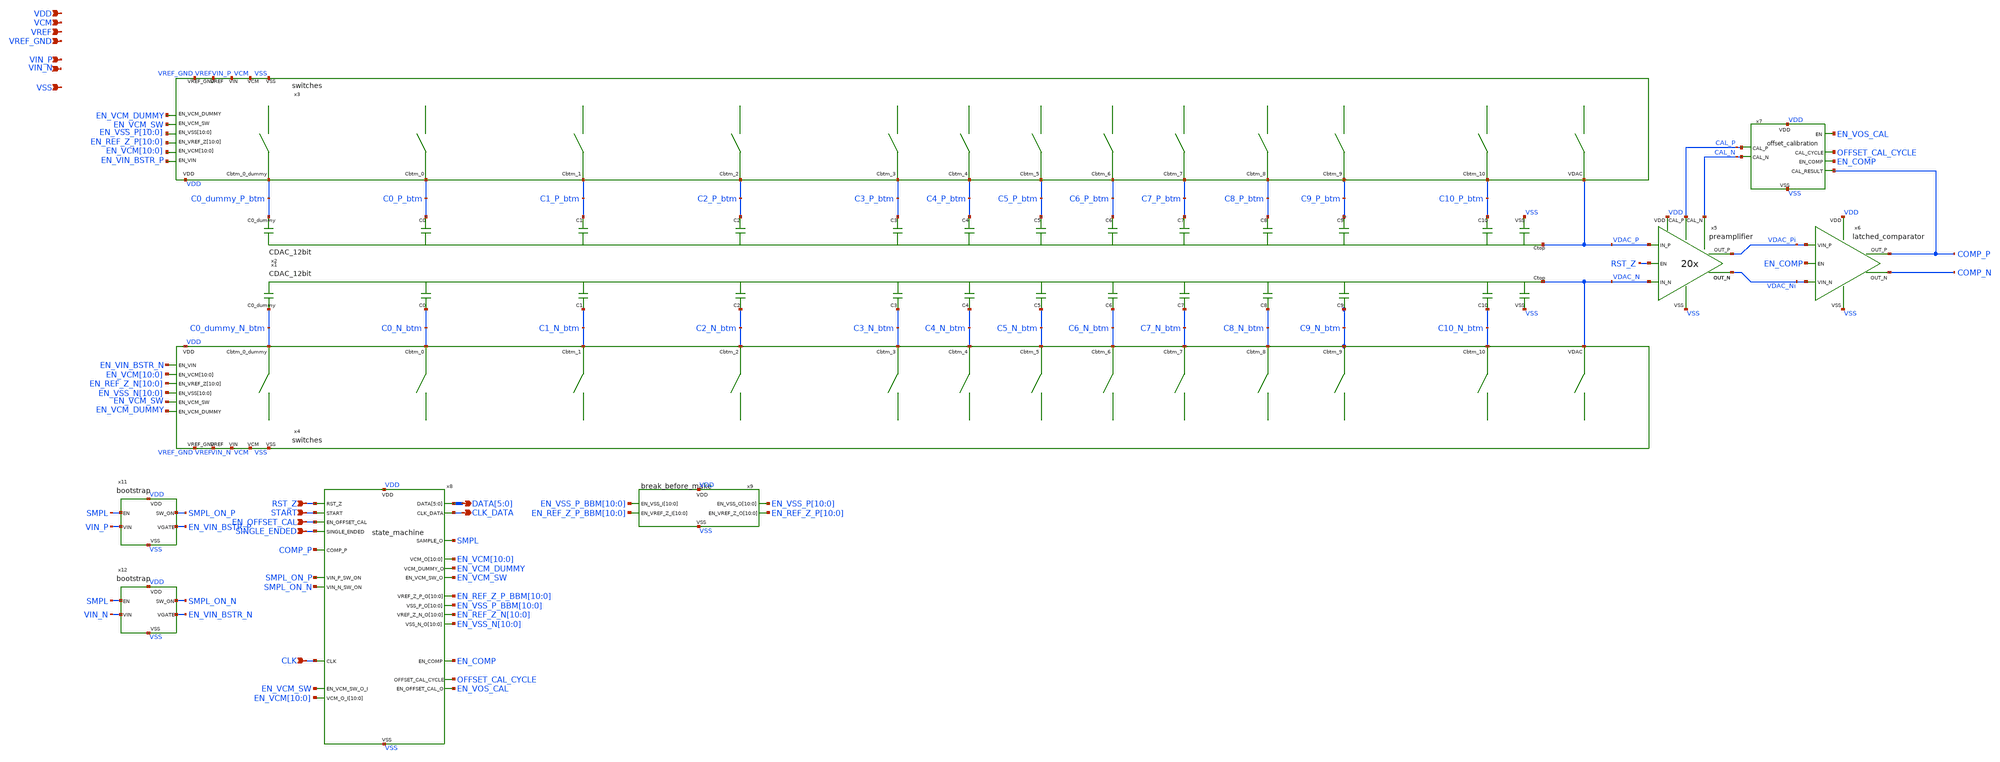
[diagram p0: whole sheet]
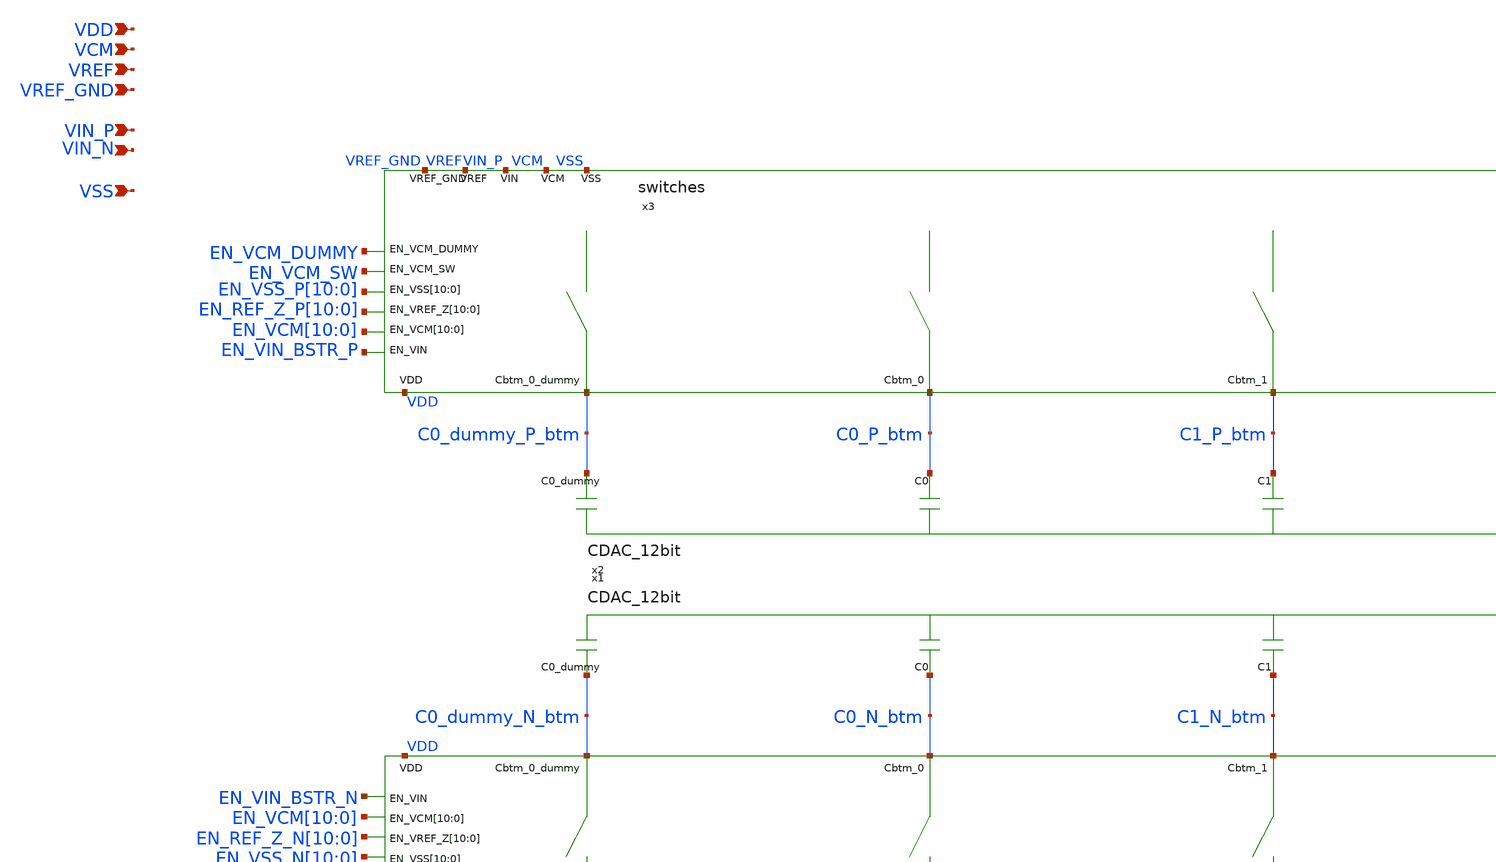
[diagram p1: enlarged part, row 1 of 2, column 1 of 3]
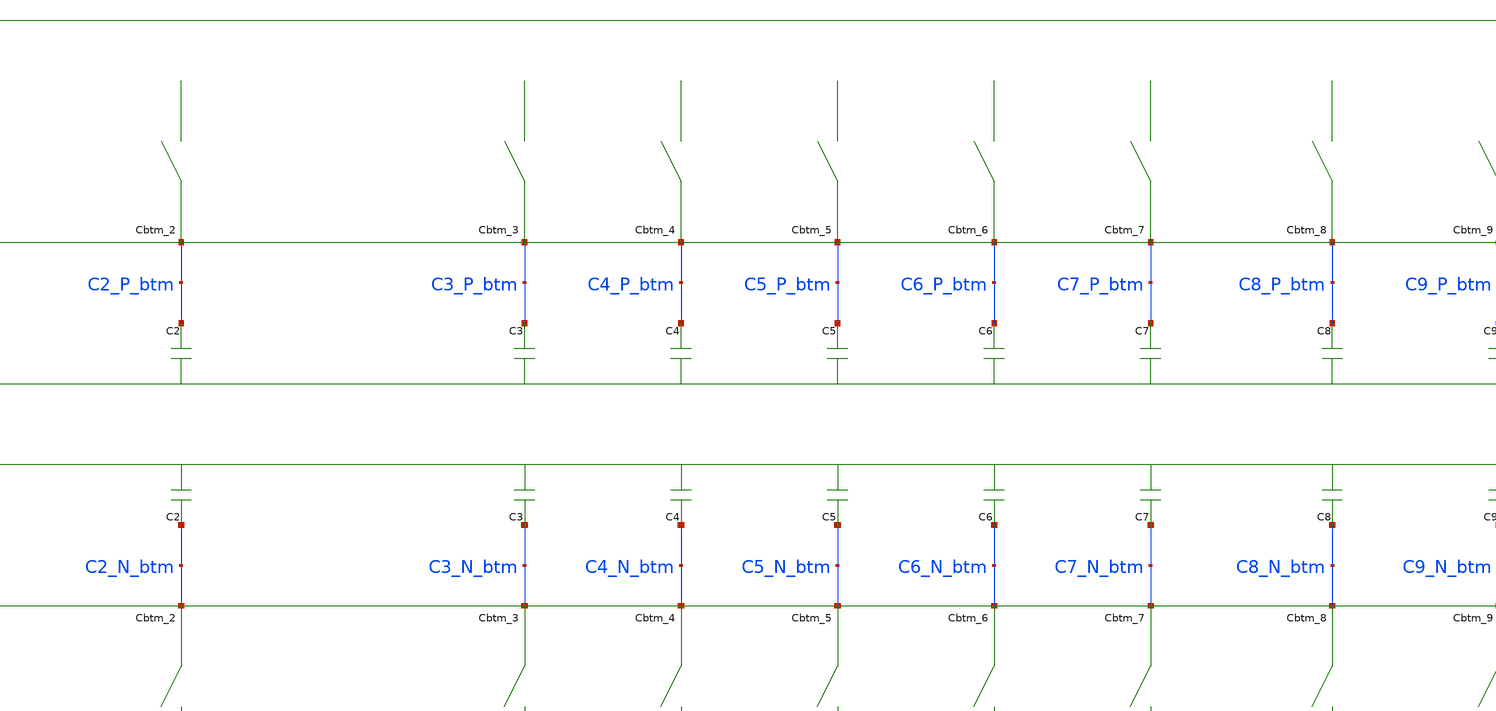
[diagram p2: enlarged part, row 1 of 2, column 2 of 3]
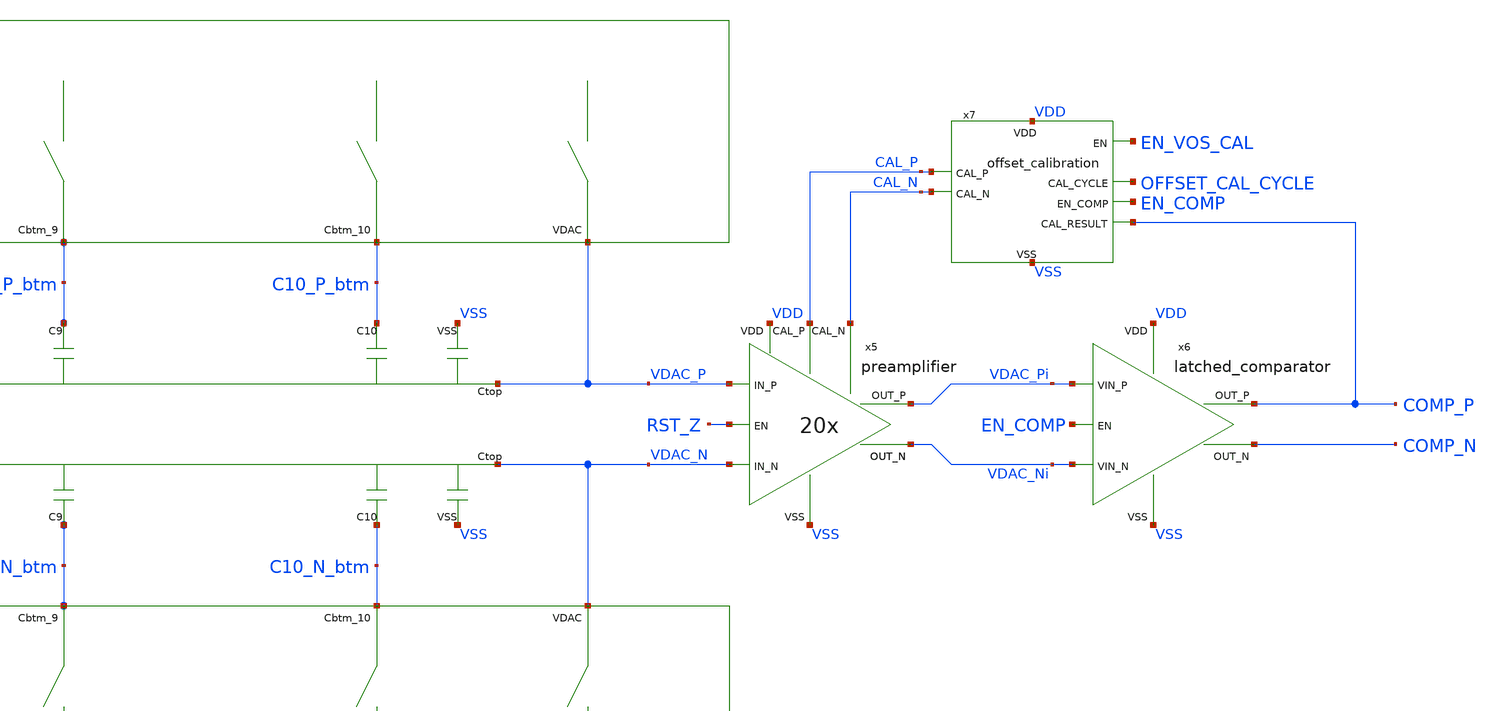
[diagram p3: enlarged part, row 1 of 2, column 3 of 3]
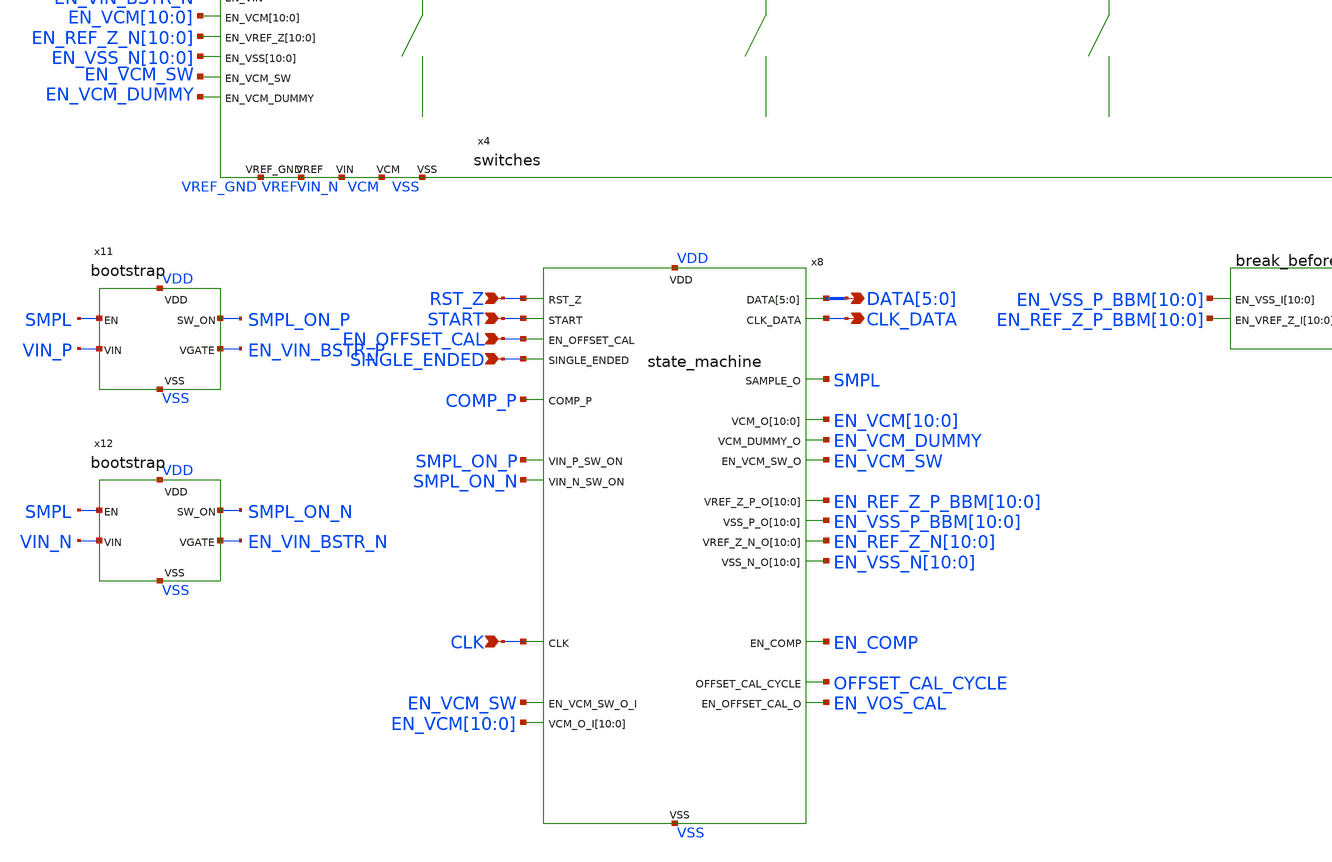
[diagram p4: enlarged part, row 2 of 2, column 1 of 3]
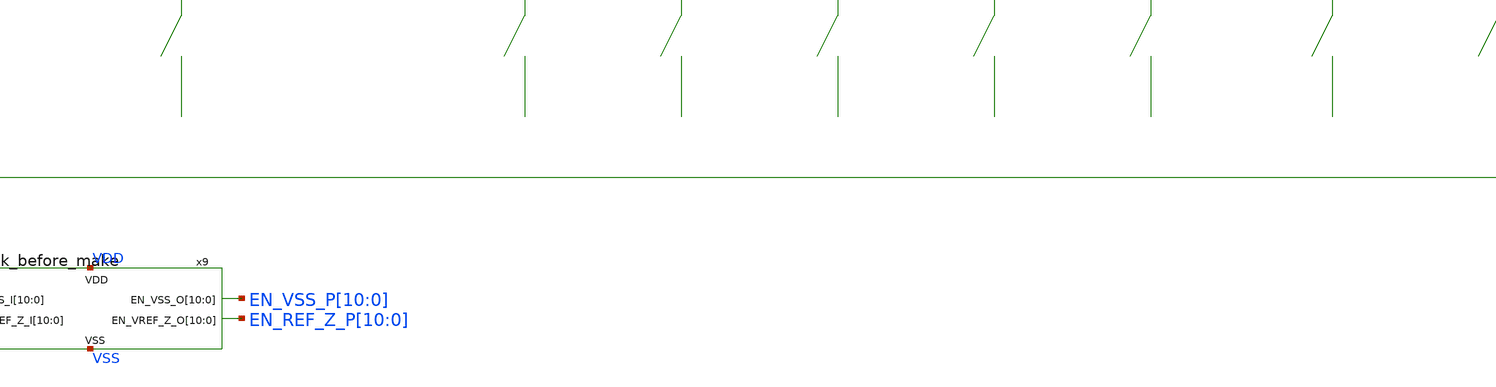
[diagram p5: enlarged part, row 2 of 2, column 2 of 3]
** sch_path: schematic/SAR_ADC_12bit.sch
**.subckt SAR_ADC_12bit VIN_P VDD VREF VCM VSS VIN_N RST_Z START CLK_DATA
*+ DATA[5],DATA[4],DATA[3],DATA[2],DATA[1],DATA[0] EN_OFFSET_CAL CLK VREF_GND SINGLE_ENDED
*.ipin VIN_P
*.ipin VDD
*.ipin VREF
*.ipin VCM
*.ipin VSS
*.ipin VIN_N
*.ipin RST_Z
*.ipin START
*.opin CLK_DATA
*.opin DATA[5],DATA[4],DATA[3],DATA[2],DATA[1],DATA[0]
*.ipin EN_OFFSET_CAL
*.ipin CLK
*.ipin VREF_GND
*.ipin SINGLE_ENDED
x1 C0_dummy_N_btm C0_N_btm C1_N_btm C2_N_btm C3_N_btm C4_N_btm C5_N_btm C6_N_btm C7_N_btm C8_N_btm
+ C9_N_btm C10_N_btm VDAC_N VSS CDAC_12bit
x2 C0_dummy_P_btm C0_P_btm C1_P_btm C2_P_btm C3_P_btm C4_P_btm C5_P_btm C6_P_btm C7_P_btm C8_P_btm
+ C9_P_btm C10_P_btm VDAC_P VSS CDAC_12bit
x3 VCM VREF_GND VREF VIN_P EN_VIN_BSTR_P EN_REF_Z_P[10] EN_REF_Z_P[9] EN_REF_Z_P[8] EN_REF_Z_P[7]
+ EN_REF_Z_P[6] EN_REF_Z_P[5] EN_REF_Z_P[4] EN_REF_Z_P[3] EN_REF_Z_P[2] EN_REF_Z_P[1] EN_REF_Z_P[0] EN_VSS_P[10]
+ EN_VSS_P[9] EN_VSS_P[8] EN_VSS_P[7] EN_VSS_P[6] EN_VSS_P[5] EN_VSS_P[4] EN_VSS_P[3] EN_VSS_P[2] EN_VSS_P[1]
+ EN_VSS_P[0] EN_VCM[10] EN_VCM[9] EN_VCM[8] EN_VCM[7] EN_VCM[6] EN_VCM[5] EN_VCM[4] EN_VCM[3] EN_VCM[2]
+ EN_VCM[1] EN_VCM[0] EN_VCM_SW EN_VCM_DUMMY C8_P_btm C7_P_btm C0_P_btm C6_P_btm C5_P_btm C0_dummy_P_btm
+ C4_P_btm C3_P_btm VDAC_P C10_P_btm C9_P_btm C2_P_btm C1_P_btm VDD VSS switches
x4 VCM VREF_GND VREF VIN_N EN_VIN_BSTR_N EN_REF_Z_N[10] EN_REF_Z_N[9] EN_REF_Z_N[8] EN_REF_Z_N[7]
+ EN_REF_Z_N[6] EN_REF_Z_N[5] EN_REF_Z_N[4] EN_REF_Z_N[3] EN_REF_Z_N[2] EN_REF_Z_N[1] EN_REF_Z_N[0] EN_VSS_N[10]
+ EN_VSS_N[9] EN_VSS_N[8] EN_VSS_N[7] EN_VSS_N[6] EN_VSS_N[5] EN_VSS_N[4] EN_VSS_N[3] EN_VSS_N[2] EN_VSS_N[1]
+ EN_VSS_N[0] EN_VCM[10] EN_VCM[9] EN_VCM[8] EN_VCM[7] EN_VCM[6] EN_VCM[5] EN_VCM[4] EN_VCM[3] EN_VCM[2]
+ EN_VCM[1] EN_VCM[0] EN_VCM_SW EN_VCM_DUMMY C8_N_btm C7_N_btm C0_N_btm C6_N_btm C5_N_btm C0_dummy_N_btm
+ C4_N_btm C3_N_btm VDAC_N C10_N_btm C9_N_btm C2_N_btm C1_N_btm VDD VSS switches
x5 VDAC_N VDAC_P VDD RST_Z VDAC_Pi VDAC_Ni VSS CAL_P CAL_N preamplifier
x6 VDD VDAC_Pi VDAC_Ni EN_COMP COMP_P COMP_N VSS latched_comparator
x7 VDD COMP_P EN_COMP CAL_P CAL_N EN_VOS_CAL VSS OFFSET_CAL_CYCLE offset_calibration
x8 VDD VSS RST_Z START COMP_P SMPL EN_VCM[10] EN_VCM[9] EN_VCM[8] EN_VCM[7] EN_VCM[6] EN_VCM[5]
+ EN_VCM[4] EN_VCM[3] EN_VCM[2] EN_VCM[1] EN_VCM[0] EN_COMP SMPL_ON_P SMPL_ON_N EN_VCM_DUMMY EN_VCM_SW
+ EN_OFFSET_CAL OFFSET_CAL_CYCLE EN_VOS_CAL CLK_DATA DATA[5] DATA[4] DATA[3] DATA[2] DATA[1] DATA[0] EN_VSS_N[10]
+ EN_VSS_N[9] EN_VSS_N[8] EN_VSS_N[7] EN_VSS_N[6] EN_VSS_N[5] EN_VSS_N[4] EN_VSS_N[3] EN_VSS_N[2] EN_VSS_N[1]
+ EN_VSS_N[0] EN_REF_Z_N[10] EN_REF_Z_N[9] EN_REF_Z_N[8] EN_REF_Z_N[7] EN_REF_Z_N[6] EN_REF_Z_N[5] EN_REF_Z_N[4]
+ EN_REF_Z_N[3] EN_REF_Z_N[2] EN_REF_Z_N[1] EN_REF_Z_N[0] EN_VSS_P_BBM[10] EN_VSS_P_BBM[9] EN_VSS_P_BBM[8]
+ EN_VSS_P_BBM[7] EN_VSS_P_BBM[6] EN_VSS_P_BBM[5] EN_VSS_P_BBM[4] EN_VSS_P_BBM[3] EN_VSS_P_BBM[2] EN_VSS_P_BBM[1]
+ EN_VSS_P_BBM[0] EN_REF_Z_P_BBM[10] EN_REF_Z_P_BBM[9] EN_REF_Z_P_BBM[8] EN_REF_Z_P_BBM[7] EN_REF_Z_P_BBM[6]
+ EN_REF_Z_P_BBM[5] EN_REF_Z_P_BBM[4] EN_REF_Z_P_BBM[3] EN_REF_Z_P_BBM[2] EN_REF_Z_P_BBM[1] EN_REF_Z_P_BBM[0] CLK
+ EN_VCM_SW EN_VCM[10] EN_VCM[9] EN_VCM[8] EN_VCM[7] EN_VCM[6] EN_VCM[5] EN_VCM[4] EN_VCM[3] EN_VCM[2]
+ EN_VCM[1] EN_VCM[0] SINGLE_ENDED state_machine
x11 VDD VSS VIN_P SMPL_ON_P SMPL EN_VIN_BSTR_P bootstrap
x12 VDD VSS VIN_N SMPL_ON_N SMPL EN_VIN_BSTR_N bootstrap
x9 EN_VSS_P_BBM[10] EN_VSS_P_BBM[9] EN_VSS_P_BBM[8] EN_VSS_P_BBM[7] EN_VSS_P_BBM[6] EN_VSS_P_BBM[5]
+ EN_VSS_P_BBM[4] EN_VSS_P_BBM[3] EN_VSS_P_BBM[2] EN_VSS_P_BBM[1] EN_VSS_P_BBM[0] VDD VSS EN_VSS_P[10] EN_VSS_P[9]
+ EN_VSS_P[8] EN_VSS_P[7] EN_VSS_P[6] EN_VSS_P[5] EN_VSS_P[4] EN_VSS_P[3] EN_VSS_P[2] EN_VSS_P[1] EN_VSS_P[0]
+ EN_REF_Z_P[10] EN_REF_Z_P[9] EN_REF_Z_P[8] EN_REF_Z_P[7] EN_REF_Z_P[6] EN_REF_Z_P[5] EN_REF_Z_P[4] EN_REF_Z_P[3]
+ EN_REF_Z_P[2] EN_REF_Z_P[1] EN_REF_Z_P[0] EN_REF_Z_P_BBM[10] EN_REF_Z_P_BBM[9] EN_REF_Z_P_BBM[8]
+ EN_REF_Z_P_BBM[7] EN_REF_Z_P_BBM[6] EN_REF_Z_P_BBM[5] EN_REF_Z_P_BBM[4] EN_REF_Z_P_BBM[3] EN_REF_Z_P_BBM[2]
+ EN_REF_Z_P_BBM[1] EN_REF_Z_P_BBM[0] break_before_make
**.ends
.end
